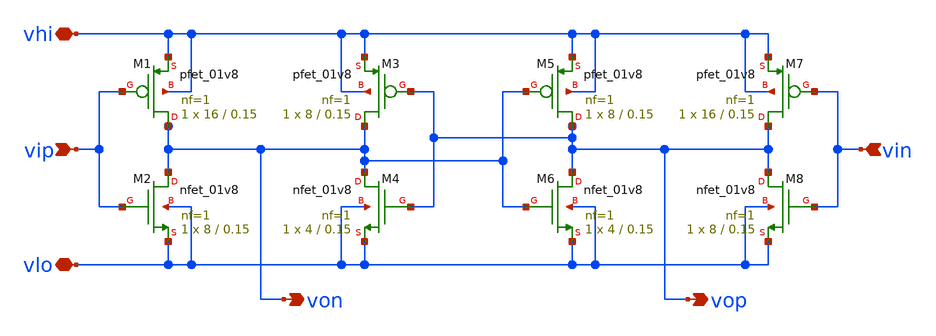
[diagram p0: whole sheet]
** sch_path: xschem/xcpinv_cell.sch
**.subckt xcpinv_cell vhi vlo vip vin von vop
*.iopin vhi
*.iopin vlo
*.ipin vip
*.ipin vin
*.opin von
*.opin vop
XM1 von vip vhi vhi sky130_fd_pr__pfet_01v8 L=0.15 W=16 nf=1 ad='int((nf+1)/2) * W/nf * 0.29' as='int((nf+2)/2) * W/nf * 0.29'
+ pd='2*int((nf+1)/2) * (W/nf + 0.29)' ps='2*int((nf+2)/2) * (W/nf + 0.29)' nrd='0.29 / W' nrs='0.29 / W'
+ sa=0 sb=0 sd=0 mult=1 m=1
XM2 von vip vlo vlo sky130_fd_pr__nfet_01v8 L=0.15 W=8 nf=1 ad='int((nf+1)/2) * W/nf * 0.29' as='int((nf+2)/2) * W/nf * 0.29'
+ pd='2*int((nf+1)/2) * (W/nf + 0.29)' ps='2*int((nf+2)/2) * (W/nf + 0.29)' nrd='0.29 / W' nrs='0.29 / W'
+ sa=0 sb=0 sd=0 mult=1 m=1
XM3 von vop vhi vhi sky130_fd_pr__pfet_01v8 L=0.15 W=8 nf=1 ad='int((nf+1)/2) * W/nf * 0.29' as='int((nf+2)/2) * W/nf * 0.29'
+ pd='2*int((nf+1)/2) * (W/nf + 0.29)' ps='2*int((nf+2)/2) * (W/nf + 0.29)' nrd='0.29 / W' nrs='0.29 / W'
+ sa=0 sb=0 sd=0 mult=1 m=1
XM4 von vop vlo vlo sky130_fd_pr__nfet_01v8 L=0.15 W=4 nf=1 ad='int((nf+1)/2) * W/nf * 0.29' as='int((nf+2)/2) * W/nf * 0.29'
+ pd='2*int((nf+1)/2) * (W/nf + 0.29)' ps='2*int((nf+2)/2) * (W/nf + 0.29)' nrd='0.29 / W' nrs='0.29 / W'
+ sa=0 sb=0 sd=0 mult=1 m=1
XM5 vop von vhi vhi sky130_fd_pr__pfet_01v8 L=0.15 W=8 nf=1 ad='int((nf+1)/2) * W/nf * 0.29' as='int((nf+2)/2) * W/nf * 0.29'
+ pd='2*int((nf+1)/2) * (W/nf + 0.29)' ps='2*int((nf+2)/2) * (W/nf + 0.29)' nrd='0.29 / W' nrs='0.29 / W'
+ sa=0 sb=0 sd=0 mult=1 m=1
XM6 vop von vlo vlo sky130_fd_pr__nfet_01v8 L=0.15 W=4 nf=1 ad='int((nf+1)/2) * W/nf * 0.29' as='int((nf+2)/2) * W/nf * 0.29'
+ pd='2*int((nf+1)/2) * (W/nf + 0.29)' ps='2*int((nf+2)/2) * (W/nf + 0.29)' nrd='0.29 / W' nrs='0.29 / W'
+ sa=0 sb=0 sd=0 mult=1 m=1
XM7 vop vin vhi vhi sky130_fd_pr__pfet_01v8 L=0.15 W=16 nf=1 ad='int((nf+1)/2) * W/nf * 0.29' as='int((nf+2)/2) * W/nf * 0.29'
+ pd='2*int((nf+1)/2) * (W/nf + 0.29)' ps='2*int((nf+2)/2) * (W/nf + 0.29)' nrd='0.29 / W' nrs='0.29 / W'
+ sa=0 sb=0 sd=0 mult=1 m=1
XM8 vop vin vlo vlo sky130_fd_pr__nfet_01v8 L=0.15 W=8 nf=1 ad='int((nf+1)/2) * W/nf * 0.29' as='int((nf+2)/2) * W/nf * 0.29'
+ pd='2*int((nf+1)/2) * (W/nf + 0.29)' ps='2*int((nf+2)/2) * (W/nf + 0.29)' nrd='0.29 / W' nrs='0.29 / W'
+ sa=0 sb=0 sd=0 mult=1 m=1
**.ends
.end
